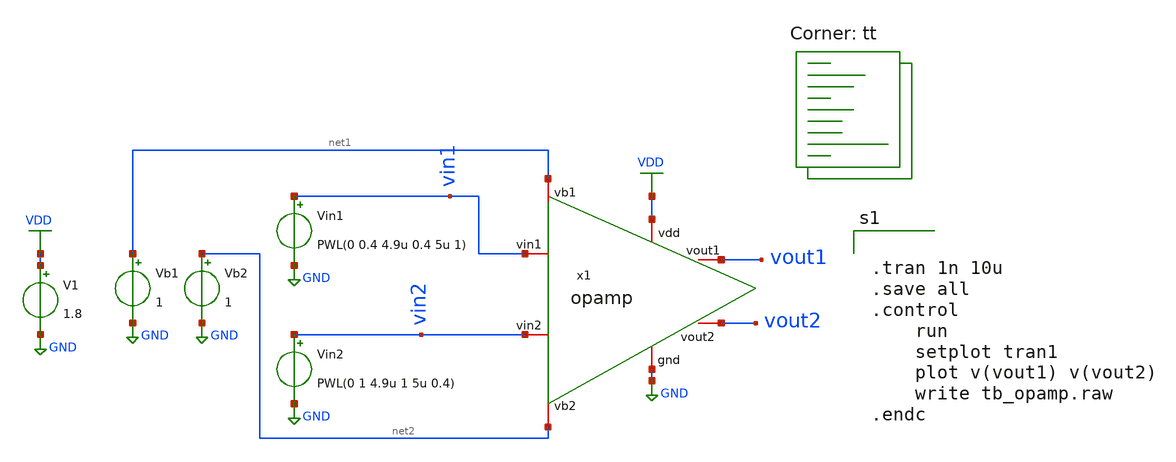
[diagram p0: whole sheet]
** sch_path: DIA3/opamp_final/tb_opamp.sch
**.subckt tb_opamp
x1 VDD net1 vin2 vin1 vout2 vout1 net2 GND opamp
V1 VDD GND 1.8
Vin1 vin1 GND PWL(0 0.4 4.9u 0.4 5u 1)
Vin2 vin2 GND PWL(0 1 4.9u 1 5u 0.4)
Vb1 net1 GND 1
Vb2 net2 GND 1
**** begin user architecture code
.lib $::SKYWATER_MODELS/sky130.lib.spice tt


.tran 1n 10u
.save all
.control
	run
	setplot tran1
	plot v(vout1) v(vout2)
	write tb_opamp.raw
.endc



**** end user architecture code
**.ends

* expanding   symbol:  opamp.sym # of pins=8
** sym_path: DIA3/opamp_final/opamp.sym
** sch_path: DIA3/opamp_final/opamp.sch
.subckt opamp vdd vb1 vin2 vin1 vout2 vout1 vb2 gnd
*.iopin vdd
*.iopin gnd
*.iopin vout1
*.iopin vout2
*.iopin vin1
*.iopin vin2
*.iopin vb1
*.iopin vb2
XM1 X vb1 vdd vdd sky130_fd_pr__pfet_01v8 L=0.15 W=2.27 nf=1 ad='int((nf+1)/2) * W/nf * 0.29' as='int((nf+2)/2) * W/nf * 0.29'
+ pd='2*int((nf+1)/2) * (W/nf + 0.29)' ps='2*int((nf+2)/2) * (W/nf + 0.29)' nrd='0.29 / W' nrs='0.29 / W'
+ sa=0 sb=0 sd=0 mult=1 m=1
XM2 Y vb1 vdd vdd sky130_fd_pr__pfet_01v8 L=0.15 W=2.27 nf=1 ad='int((nf+1)/2) * W/nf * 0.29' as='int((nf+2)/2) * W/nf * 0.29'
+ pd='2*int((nf+1)/2) * (W/nf + 0.29)' ps='2*int((nf+2)/2) * (W/nf + 0.29)' nrd='0.29 / W' nrs='0.29 / W'
+ sa=0 sb=0 sd=0 mult=1 m=1
XM3 X vin2 net1 gnd sky130_fd_pr__nfet_01v8 L=0.15 W=0.86 nf=1 ad='int((nf+1)/2) * W/nf * 0.29' as='int((nf+2)/2) * W/nf * 0.29'
+ pd='2*int((nf+1)/2) * (W/nf + 0.29)' ps='2*int((nf+2)/2) * (W/nf + 0.29)' nrd='0.29 / W' nrs='0.29 / W'
+ sa=0 sb=0 sd=0 mult=1 m=1
XM4 Y vin1 net1 gnd sky130_fd_pr__nfet_01v8 L=0.15 W=0.86 nf=1 ad='int((nf+1)/2) * W/nf * 0.29' as='int((nf+2)/2) * W/nf * 0.29'
+ pd='2*int((nf+1)/2) * (W/nf + 0.29)' ps='2*int((nf+2)/2) * (W/nf + 0.29)' nrd='0.29 / W' nrs='0.29 / W'
+ sa=0 sb=0 sd=0 mult=1 m=1
XM5 net1 net2 gnd gnd sky130_fd_pr__nfet_01v8 L=0.15 W=0.49 nf=1 ad='int((nf+1)/2) * W/nf * 0.29' as='int((nf+2)/2) * W/nf * 0.29'
+ pd='2*int((nf+1)/2) * (W/nf + 0.29)' ps='2*int((nf+2)/2) * (W/nf + 0.29)' nrd='0.29 / W' nrs='0.29 / W'
+ sa=0 sb=0 sd=0 mult=1 m=1
XM6 vout1 Y vdd vdd sky130_fd_pr__pfet_01v8 L=0.15 W=56.9 nf=1 ad='int((nf+1)/2) * W/nf * 0.29' as='int((nf+2)/2) * W/nf * 0.29'
+ pd='2*int((nf+1)/2) * (W/nf + 0.29)' ps='2*int((nf+2)/2) * (W/nf + 0.29)' nrd='0.29 / W' nrs='0.29 / W'
+ sa=0 sb=0 sd=0 mult=1 m=1
XM7 vout2 X vdd vdd sky130_fd_pr__pfet_01v8 L=0.15 W=56.9 nf=1 ad='int((nf+1)/2) * W/nf * 0.29' as='int((nf+2)/2) * W/nf * 0.29'
+ pd='2*int((nf+1)/2) * (W/nf + 0.29)' ps='2*int((nf+2)/2) * (W/nf + 0.29)' nrd='0.29 / W' nrs='0.29 / W'
+ sa=0 sb=0 sd=0 mult=1 m=1
XM8 vout1 vb2 gnd gnd sky130_fd_pr__nfet_01v8 L=0.15 W=1.34 nf=1 ad='int((nf+1)/2) * W/nf * 0.29' as='int((nf+2)/2) * W/nf * 0.29'
+ pd='2*int((nf+1)/2) * (W/nf + 0.29)' ps='2*int((nf+2)/2) * (W/nf + 0.29)' nrd='0.29 / W' nrs='0.29 / W'
+ sa=0 sb=0 sd=0 mult=1 m=1
XM9 vout2 vb2 gnd gnd sky130_fd_pr__nfet_01v8 L=0.15 W=1.34 nf=1 ad='int((nf+1)/2) * W/nf * 0.29' as='int((nf+2)/2) * W/nf * 0.29'
+ pd='2*int((nf+1)/2) * (W/nf + 0.29)' ps='2*int((nf+2)/2) * (W/nf + 0.29)' nrd='0.29 / W' nrs='0.29 / W'
+ sa=0 sb=0 sd=0 mult=1 m=1
XM10 net2 net2 gnd gnd sky130_fd_pr__nfet_01v8 L=0.15 W=29 nf=1 ad='int((nf+1)/2) * W/nf * 0.29' as='int((nf+2)/2) * W/nf * 0.29'
+ pd='2*int((nf+1)/2) * (W/nf + 0.29)' ps='2*int((nf+2)/2) * (W/nf + 0.29)' nrd='0.29 / W' nrs='0.29 / W'
+ sa=0 sb=0 sd=0 mult=1 m=1
XR2 net2 vdd sky130_fd_pr__res_generic_po W=1 L=3.95 m=1
.ends

.GLOBAL GND
.GLOBAL VDD
.end
